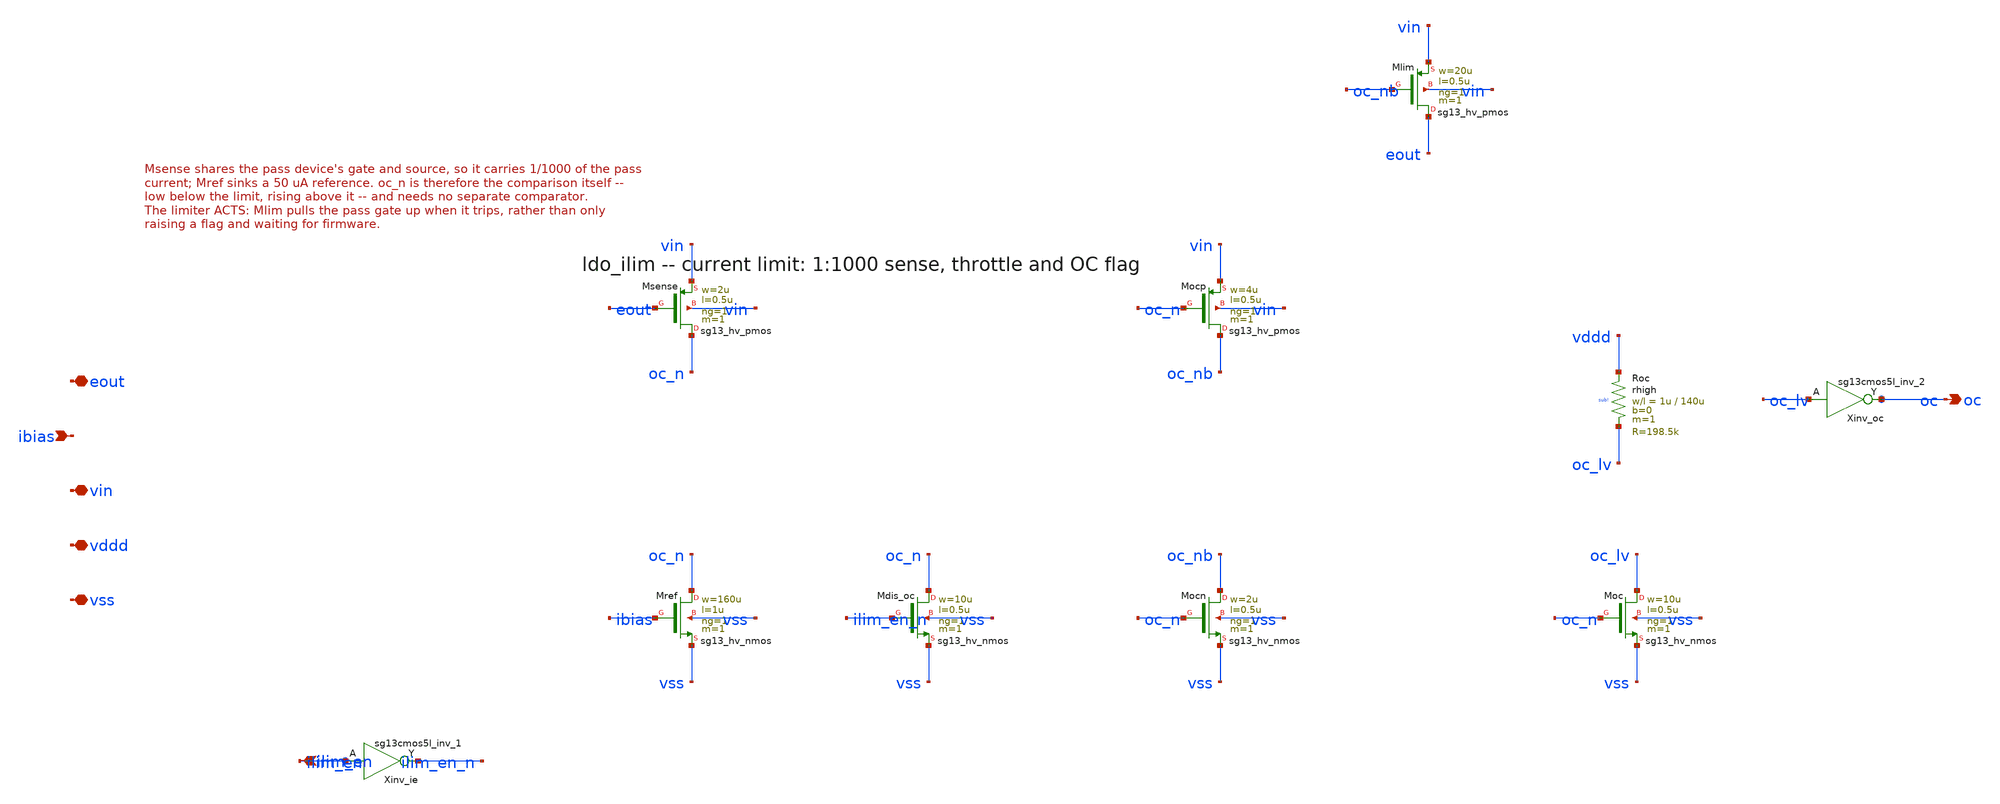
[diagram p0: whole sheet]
** sch_path: xschem/ldo_ilim.sch
**.subckt ldo_ilim eout ibias ilim_en oc vin vddd vss
*.iopin eout
*.ipin ibias
*.ipin ilim_en
*.opin oc
*.iopin vin
*.iopin vddd
*.iopin vss
XMsense oc_n eout vin vin sg13_hv_pmos w=2u l=0.5u ng=1 m=1 mm_ok=1
XMref oc_n ibias vss vss sg13_hv_nmos w=160u l=1u ng=1 m=1 mm_ok=1
XMdis_oc oc_n ilim_en_n vss vss sg13_hv_nmos w=10u l=0.5u ng=1 m=1 mm_ok=1
Xinv_ie ilim_en_n ilim_en vddd vss sg13cmos5l_inv_1
XMocp oc_nb oc_n vin vin sg13_hv_pmos w=4u l=0.5u ng=1 m=1 mm_ok=1
XMocn oc_nb oc_n vss vss sg13_hv_nmos w=2u l=0.5u ng=1 m=1 mm_ok=1
XMlim eout oc_nb vin vin sg13_hv_pmos w=20u l=0.5u ng=1 m=1 mm_ok=1
XRoc vddd oc_lv sub! rhigh w=1u l=140u m=1 b=0 mm_ok=1
XMoc oc_lv oc_n vss vss sg13_hv_nmos w=10u l=0.5u ng=1 m=1 mm_ok=1
Xinv_oc oc oc_lv vddd vss sg13cmos5l_inv_2
**.ends
.end
